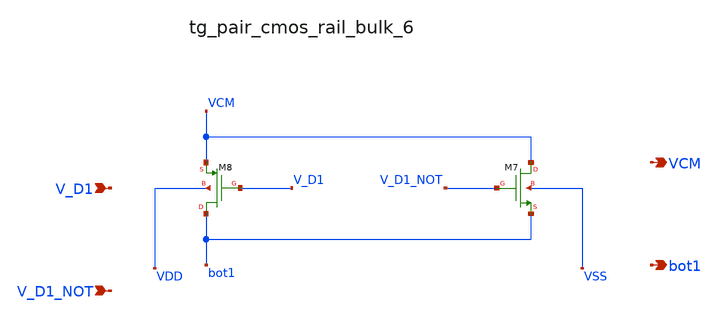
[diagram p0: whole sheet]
** sch_path: analog-db/raw/sw_003_binary_capbank/hier/blocks/tg_pair_cmos_rail_bulk_6.sch
**.subckt tg_pair_cmos_rail_bulk_6 V_D1 V_D1_NOT VCM bot1
*.ipin V_D1
*.ipin V_D1_NOT
*.opin VCM
*.opin bot1
XM7 VCM V_D1_NOT bot1 VSS sg13_lv_nmos w=x_dut_xm7_w l=x_dut_xm7_l ng=1 m=x_dut_xm7_m
XM8 bot1 V_D1 VCM VDD sg13_lv_pmos w=x_dut_xm8_w l=x_dut_xm8_l ng=1 m=x_dut_xm8_m
**.ends
.end
